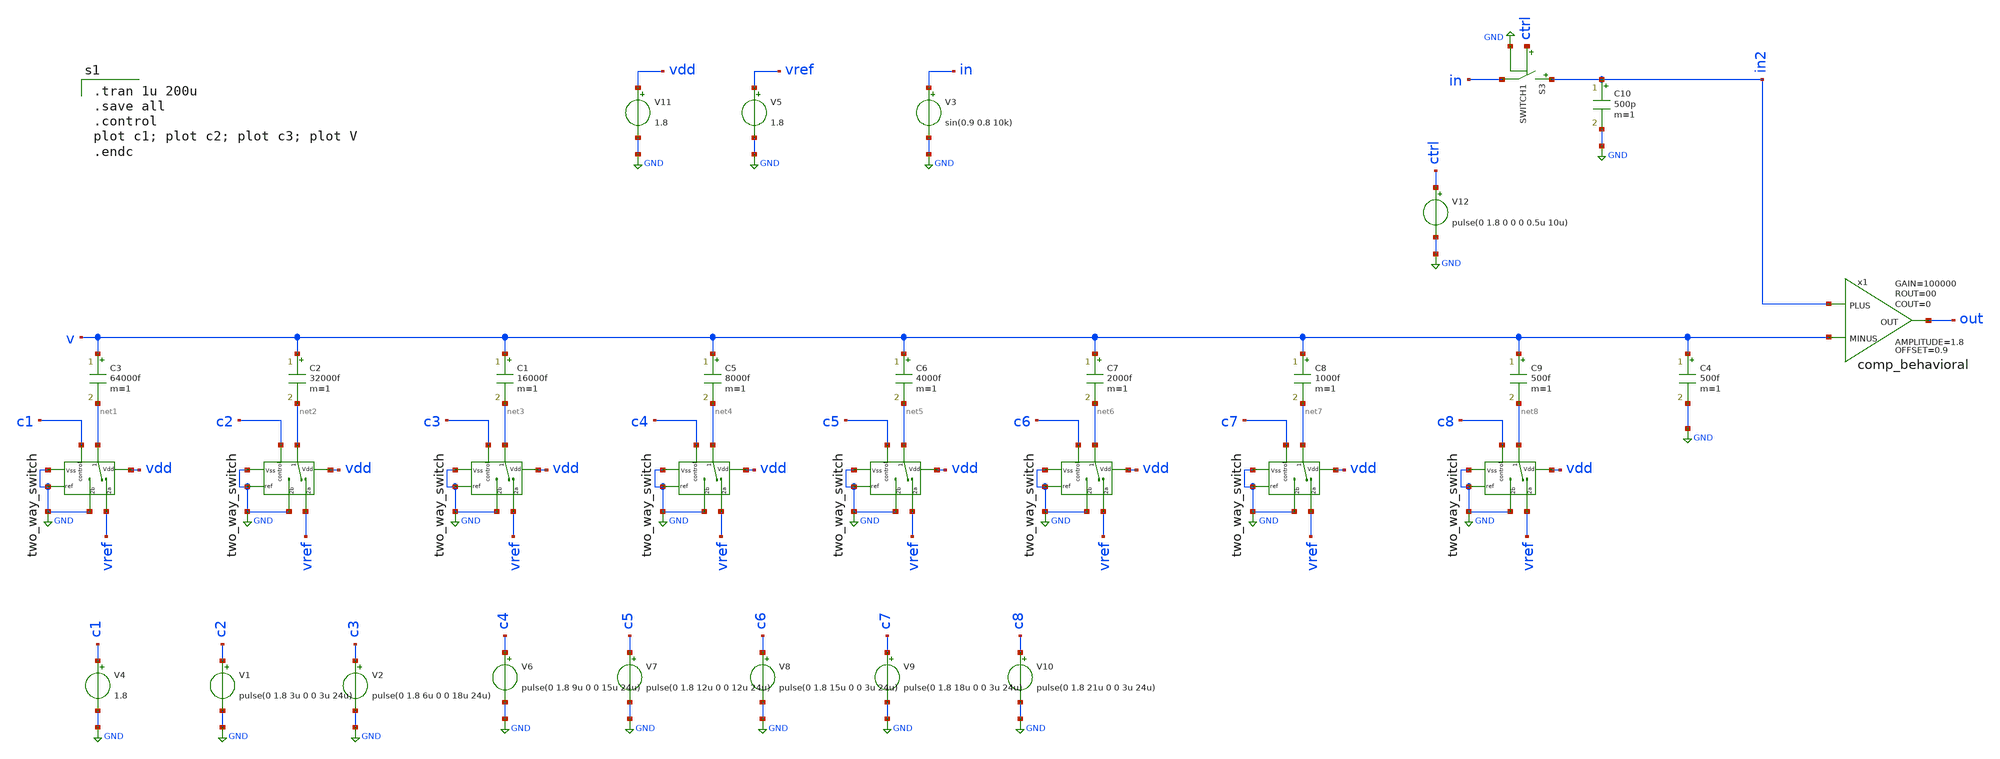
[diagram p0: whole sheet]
** sch_path: Behavioral_model/S_SARADC.sch
**.subckt S_SARADC
x1 in2 v out comp_behavioral OFFSET=0.9 AMPLITUDE=1.8 GAIN=100000 ROUT=00 COUT=0
V3 in GND sin(0.9 0.8 10k)
V4 c1 GND 1.8
C2 v net2 32000f m=1
C3 v net1 64000f m=1
C4 v GND 500f m=1
V1 c2 GND pulse(0 1.8 3u 0 0 3u 24u)
V2 c3 GND pulse(0 1.8 6u 0 0 18u 24u)
V5 vref GND 1.8
V6 c4 GND pulse(0 1.8 9u 0 0 15u 24u)
V7 c5 GND pulse(0 1.8 12u 0 0 12u 24u)
V8 c6 GND pulse(0 1.8 15u 0 0 3u 24u)
V9 c7 GND pulse(0 1.8 18u 0 0 3u 24u)
V10 c8 GND pulse(0 1.8 21u 0 0 3u 24u)
x2 net1 vdd c1 GND vref GND GND two_way_switch
V11 vdd GND 1.8
x3 net2 vdd c2 GND vref GND GND two_way_switch
C1 v net3 16000f m=1
x4 net3 vdd c3 GND vref GND GND two_way_switch
C5 v net4 8000f m=1
x5 net4 vdd c4 GND vref GND GND two_way_switch
C6 v net5 4000f m=1
x6 net5 vdd c5 GND vref GND GND two_way_switch
C7 v net6 2000f m=1
x7 net6 vdd c6 GND vref GND GND two_way_switch
C8 v net7 1000f m=1
x8 net7 vdd c7 GND vref GND GND two_way_switch
C9 v net8 500f m=1
x9 net8 vdd c8 GND vref GND GND two_way_switch
S3 in2 in ctrl GND SWITCH1
C10 in2 GND 500p m=1
V12 ctrl GND pulse(0 1.8 0 0 0 0.5u 10u)
**** begin user architecture code

.tran 1u 200u
.save all
.control
plot c1; plot c2; plot c3; plot V
.endc


.lib /usr/local/share/pdk/sky130A/libs.tech/ngspice/sky130.lib.spice tt


.model switch1 sw vt=0.1 vh=0 ron=1m roff=100G

**** end user architecture code
**.ends

* expanding   symbol:  comp_behavioral.sym # of pins=3
** sym_path: Behavioral_model/comp_behavioral.sym
** sch_path: Behavioral_model/comp_behavioral.sch
.subckt comp_behavioral PLUS MINUS OUT  OFFSET=0.9 AMPLITUDE=0.9 GAIN=100000 ROUT=00 COUT=0
*.ipin PLUS
*.ipin MINUS
*.opin OUT
B1 IOUT 0 V = {OFFSET + AMPLITUDE/2*(tanh(V(IPLUS,IMINUS)*GAIN*2/AMPLITUDE))}
V1 IPLUS PLUS 3
V2 IMINUS MINUS 3
R1 OUT IOUT {ROUT} m=1
C3 OUT 0 {COUT} m=1
.ends


* expanding   symbol:  two_way_switch.sym # of pins=7
** sym_path: Behavioral_model/two_way_switch.sym
** sch_path: Behavioral_model/two_way_switch.sch
.subckt two_way_switch 1 Vdd control ref 2a 2b Vss
*.iopin 2b
*.iopin 2a
*.ipin ref
*.iopin 1
*.ipin Vdd
*.ipin Vss
*.ipin control
S1 1 2a control ref SWITCH1
S2 1 2b net1 ref SWITCH1
x1 Vdd control net1 Vss CMOS_inverter
.ends


* expanding   symbol:  CMOS_inverter.sym # of pins=4
** sym_path: Behavioral_model/CMOS_inverter.sym
** sch_path: Behavioral_model/CMOS_inverter.sch
.subckt CMOS_inverter Vdd Q Q_N Vss
*.ipin Q
*.ipin Vdd
*.ipin Vss
*.opin Q_N
XM1 Q_N Q Vss Vss sky130_fd_pr__nfet_01v8 L=0.15 W=1 nf=1 ad='int((nf+1)/2) * W/nf * 0.29' as='int((nf+2)/2) * W/nf * 0.29'
+ pd='2*int((nf+1)/2) * (W/nf + 0.29)' ps='2*int((nf+2)/2) * (W/nf + 0.29)' nrd='0.29 / W' nrs='0.29 / W'
+ sa=0 sb=0 sd=0 mult=1 m=1
XM3 Q_N Q Vdd Vdd sky130_fd_pr__pfet_01v8 L=0.15 W=1 nf=1 ad='int((nf+1)/2) * W/nf * 0.29' as='int((nf+2)/2) * W/nf * 0.29'
+ pd='2*int((nf+1)/2) * (W/nf + 0.29)' ps='2*int((nf+2)/2) * (W/nf + 0.29)' nrd='0.29 / W' nrs='0.29 / W'
+ sa=0 sb=0 sd=0 mult=1 m=1
.ends

.GLOBAL GND
.end
